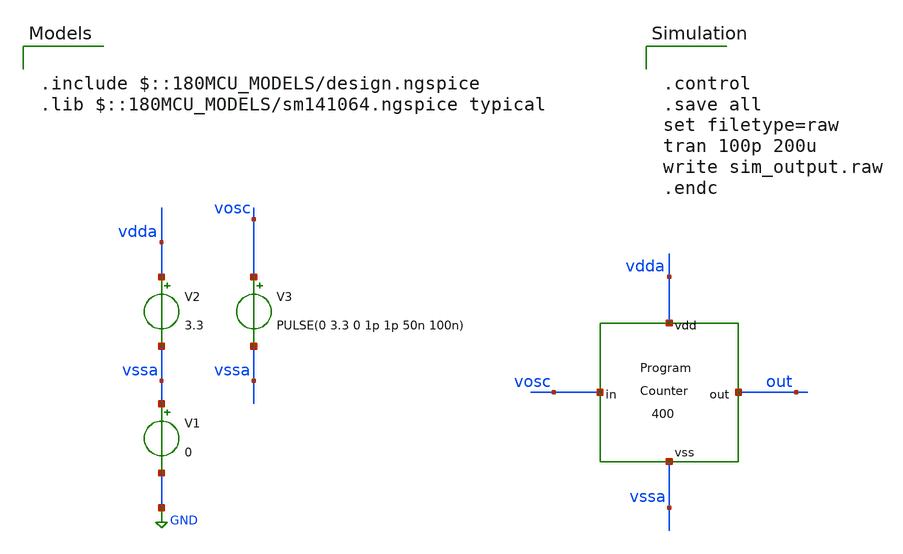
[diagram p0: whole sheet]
** sch_path: designs/libs/xp_tb_analog/tb_asc_program_counter_400/tb_asc_program_counter_400.sch
**.subckt tb_asc_program_counter_400
V1 vssa GND 0
V2 vdda vssa 3.3
V3 vosc vssa PULSE(0 3.3 0 1p 1p 50n 100n)
x1 vosc out vdda vssa asc_program_counter_400
**** begin user architecture code

.include $::180MCU_MODELS/design.ngspice
.lib $::180MCU_MODELS/sm141064.ngspice typical



.control
.save all
set filetype=raw
tran 100p 200u
write sim_output.raw
.endc


**** end user architecture code
**.ends
.GLOBAL GND
.end
